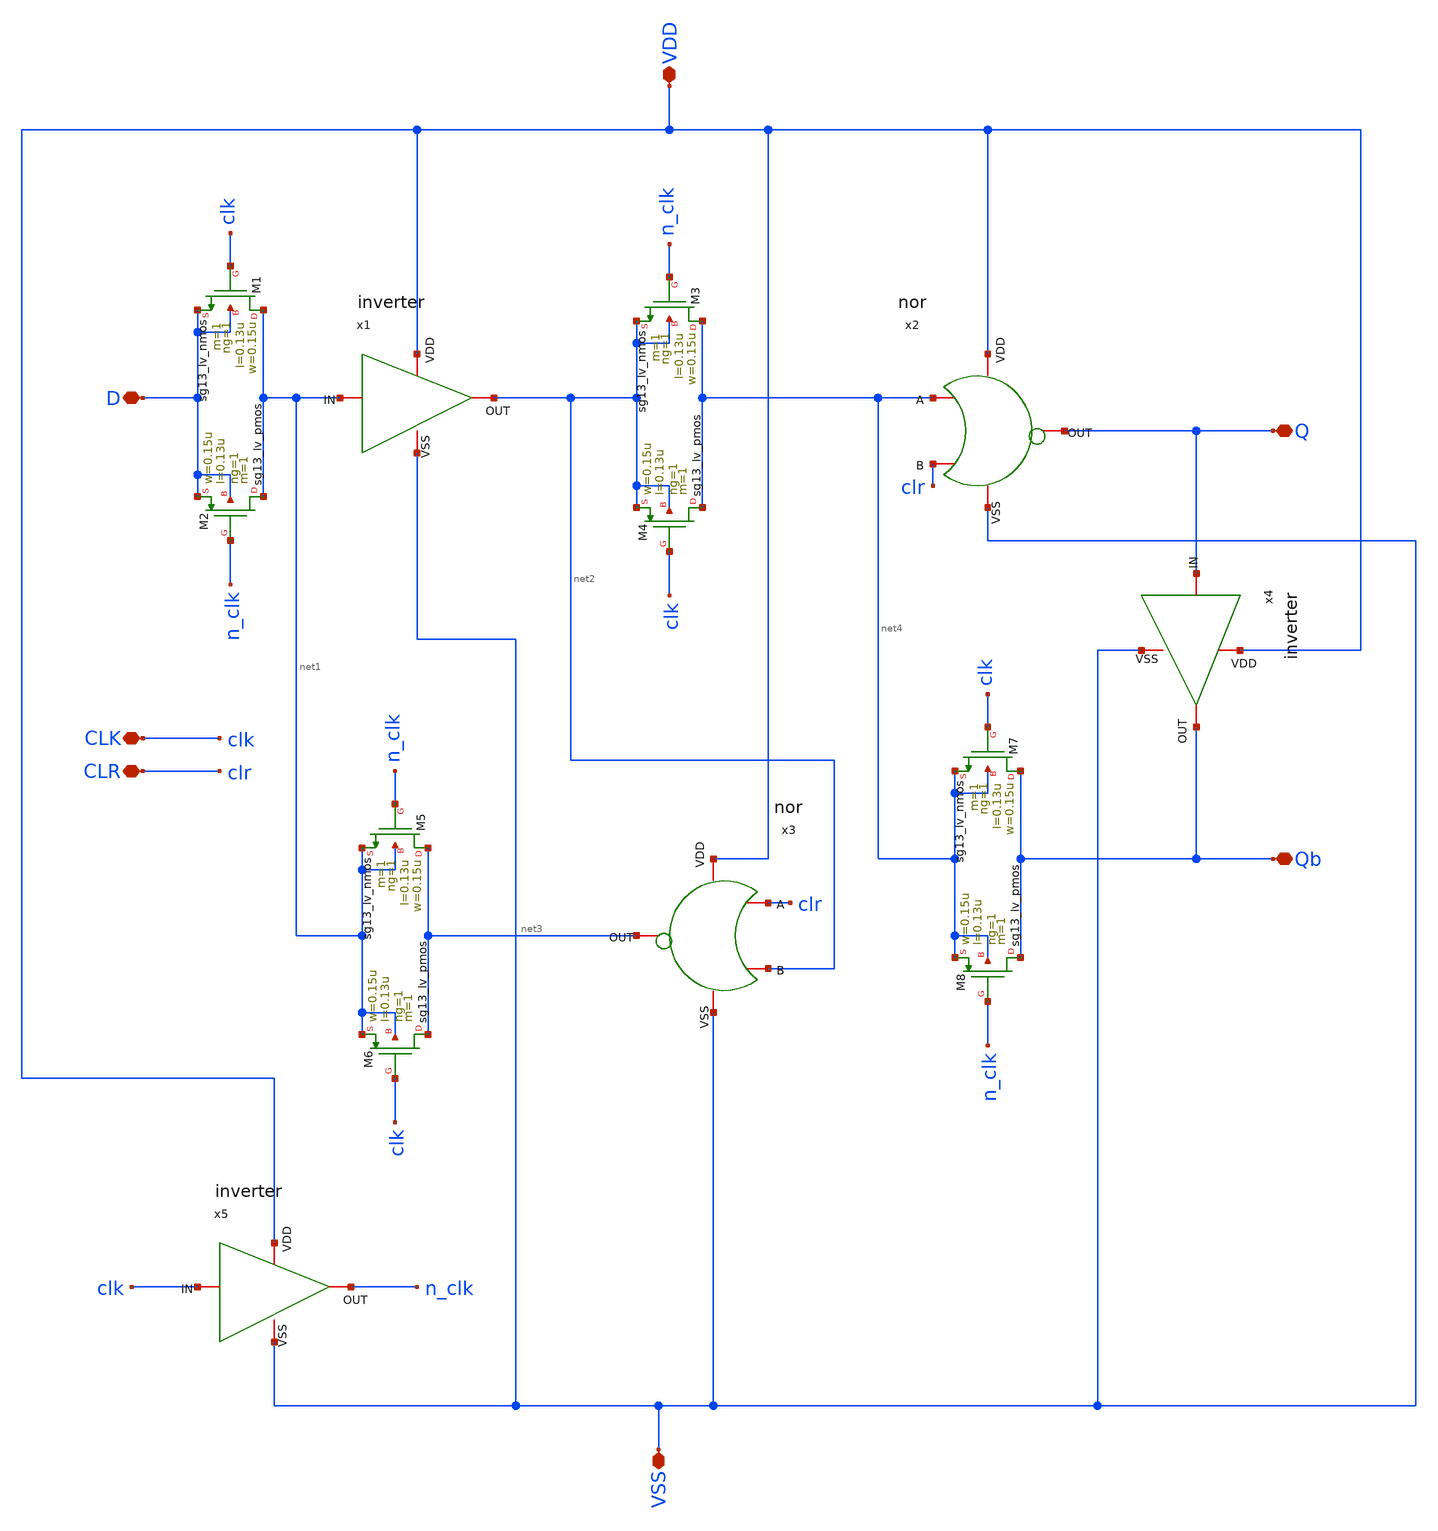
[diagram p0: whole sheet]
** sch_path: blocks/dff/dffc.sch
**.subckt dffc D Q Qb CLK CLR VDD VSS
*.iopin D
*.iopin Q
*.iopin Qb
*.iopin CLK
*.iopin CLR
*.iopin VDD
*.iopin VSS
x1 VDD net2 net1 VSS inverter
XM1 net1 clk D D sg13_lv_nmos w=0.15u l=0.13u ng=1 m=1 mm_ok=1
XM2 net1 n_clk D D sg13_lv_pmos w=0.15u l=0.13u ng=1 m=1 mm_ok=1
XM3 net4 n_clk net2 net2 sg13_lv_nmos w=0.15u l=0.13u ng=1 m=1 mm_ok=1
XM4 net4 clk net2 net2 sg13_lv_pmos w=0.15u l=0.13u ng=1 m=1 mm_ok=1
XM5 net3 n_clk net1 net1 sg13_lv_nmos w=0.15u l=0.13u ng=1 m=1 mm_ok=1
XM6 net3 clk net1 net1 sg13_lv_pmos w=0.15u l=0.13u ng=1 m=1 mm_ok=1
x4 VDD Qb Q VSS inverter
XM7 Qb clk net4 net4 sg13_lv_nmos w=0.15u l=0.13u ng=1 m=1 mm_ok=1
XM8 Qb n_clk net4 net4 sg13_lv_pmos w=0.15u l=0.13u ng=1 m=1 mm_ok=1
x5 VDD n_clk clk VSS inverter
x2 VDD clr Q net4 VSS nor
x3 VDD net2 net3 clr VSS nor
**.ends

* expanding   symbol:  blocks/inverter/inverter.sym # of pins=4
** sym_path: blocks/inverter/inverter.sym
** sch_path: blocks/inverter/inverter.sch
.subckt inverter VDD OUT IN VSS
*.iopin OUT
*.iopin VDD
*.iopin VSS
*.iopin IN
XM1 OUT IN VDD VDD sg13_lv_pmos w=1.5u l=0.15u ng=1 m=1 mm_ok=1
XM2 OUT IN VSS VSS sg13_lv_nmos w=0.75u l=0.15u ng=1 m=1 mm_ok=1
.ends


* expanding   symbol:  blocks/norgate/nor.sym # of pins=5
** sym_path: blocks/norgate/nor.sym
** sch_path: blocks/norgate/nor.sch
.subckt nor VDD B OUT A VSS
*.iopin VDD
*.iopin A
*.iopin VSS
*.iopin B
*.iopin OUT
XM1 net1 B VDD VDD sg13_lv_pmos w=3u l=0.15u ng=1 m=1 mm_ok=1
XM2 OUT A net1 VDD sg13_lv_pmos w=3u l=0.15u ng=1 m=1 mm_ok=1
XM3 OUT A VSS VSS sg13_lv_nmos w=0.75u l=0.15u ng=1 m=1 mm_ok=1
XM4 OUT B VSS VSS sg13_lv_nmos w=0.75u l=0.15u ng=1 m=1 mm_ok=1
.ends

.end
